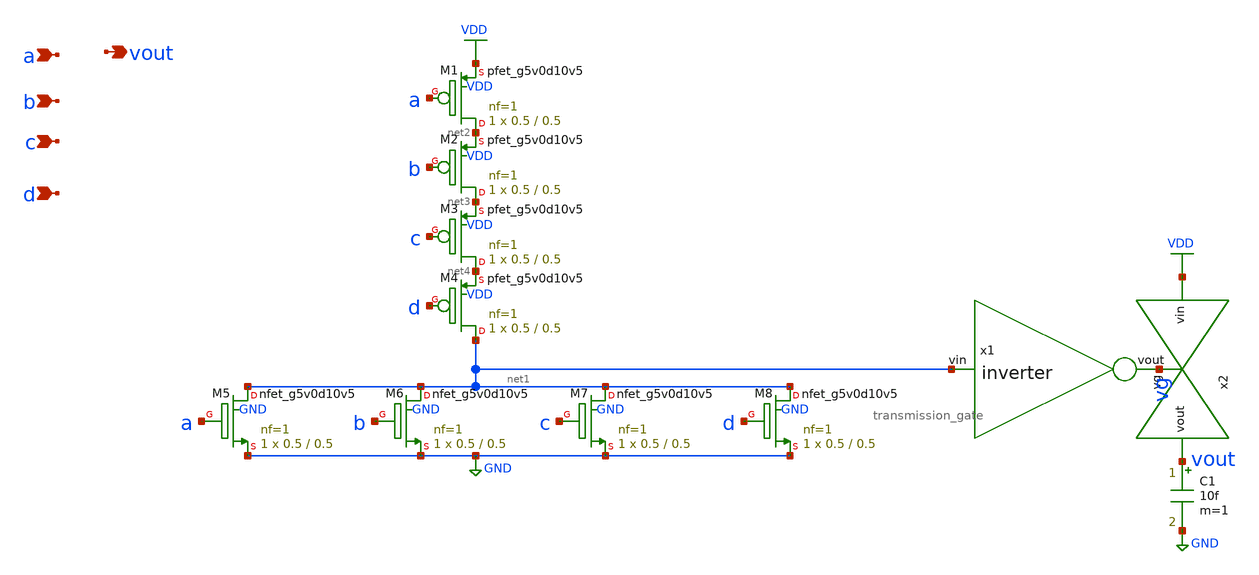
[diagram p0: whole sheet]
** sch_path: schematics/or4.sch
**.subckt or4 a b c d vout
*.ipin a
*.ipin b
*.ipin c
*.ipin d
*.opin vout
x1 vg net1 inverter
XM1 net2 a VDD VDD sky130_fd_pr__pfet_g5v0d10v5 L=0.5 W=0.5 nf=1 ad='int((nf+1)/2) * W/nf * 0.29' as='int((nf+2)/2) * W/nf * 0.29'
+ pd='2*int((nf+1)/2) * (W/nf + 0.29)' ps='2*int((nf+2)/2) * (W/nf + 0.29)' nrd='0.29 / W' nrs='0.29 / W'
+ sa=0 sb=0 sd=0 mult=1 m=1
XM5 net1 a GND GND sky130_fd_pr__nfet_g5v0d10v5 L=0.5 W=0.5 nf=1 ad='int((nf+1)/2) * W/nf * 0.29' as='int((nf+2)/2) * W/nf * 0.29'
+ pd='2*int((nf+1)/2) * (W/nf + 0.29)' ps='2*int((nf+2)/2) * (W/nf + 0.29)' nrd='0.29 / W' nrs='0.29 / W'
+ sa=0 sb=0 sd=0 mult=1 m=1
XM2 net3 b net2 VDD sky130_fd_pr__pfet_g5v0d10v5 L=0.5 W=0.5 nf=1 ad='int((nf+1)/2) * W/nf * 0.29' as='int((nf+2)/2) * W/nf * 0.29'
+ pd='2*int((nf+1)/2) * (W/nf + 0.29)' ps='2*int((nf+2)/2) * (W/nf + 0.29)' nrd='0.29 / W' nrs='0.29 / W'
+ sa=0 sb=0 sd=0 mult=1 m=1
XM3 net4 c net3 VDD sky130_fd_pr__pfet_g5v0d10v5 L=0.5 W=0.5 nf=1 ad='int((nf+1)/2) * W/nf * 0.29' as='int((nf+2)/2) * W/nf * 0.29'
+ pd='2*int((nf+1)/2) * (W/nf + 0.29)' ps='2*int((nf+2)/2) * (W/nf + 0.29)' nrd='0.29 / W' nrs='0.29 / W'
+ sa=0 sb=0 sd=0 mult=1 m=1
XM4 net1 d net4 VDD sky130_fd_pr__pfet_g5v0d10v5 L=0.5 W=0.5 nf=1 ad='int((nf+1)/2) * W/nf * 0.29' as='int((nf+2)/2) * W/nf * 0.29'
+ pd='2*int((nf+1)/2) * (W/nf + 0.29)' ps='2*int((nf+2)/2) * (W/nf + 0.29)' nrd='0.29 / W' nrs='0.29 / W'
+ sa=0 sb=0 sd=0 mult=1 m=1
XM6 net1 b GND GND sky130_fd_pr__nfet_g5v0d10v5 L=0.5 W=0.5 nf=1 ad='int((nf+1)/2) * W/nf * 0.29' as='int((nf+2)/2) * W/nf * 0.29'
+ pd='2*int((nf+1)/2) * (W/nf + 0.29)' ps='2*int((nf+2)/2) * (W/nf + 0.29)' nrd='0.29 / W' nrs='0.29 / W'
+ sa=0 sb=0 sd=0 mult=1 m=1
XM7 net1 c GND GND sky130_fd_pr__nfet_g5v0d10v5 L=0.5 W=0.5 nf=1 ad='int((nf+1)/2) * W/nf * 0.29' as='int((nf+2)/2) * W/nf * 0.29'
+ pd='2*int((nf+1)/2) * (W/nf + 0.29)' ps='2*int((nf+2)/2) * (W/nf + 0.29)' nrd='0.29 / W' nrs='0.29 / W'
+ sa=0 sb=0 sd=0 mult=1 m=1
XM8 net1 d GND GND sky130_fd_pr__nfet_g5v0d10v5 L=0.5 W=0.5 nf=1 ad='int((nf+1)/2) * W/nf * 0.29' as='int((nf+2)/2) * W/nf * 0.29'
+ pd='2*int((nf+1)/2) * (W/nf + 0.29)' ps='2*int((nf+2)/2) * (W/nf + 0.29)' nrd='0.29 / W' nrs='0.29 / W'
+ sa=0 sb=0 sd=0 mult=1 m=1
x2 VDD vout vg transmission_gate
C1 vout GND 10f m=1
**.ends

* expanding   symbol:  /media/sf_share/final_project/inverter.sym # of pins=2
** sym_path: schematics/inverter.sym
** sch_path: schematics/inverter.sch
.subckt inverter vout vin
*.ipin vin
*.opin vout
XM3 vout vin VDD VDD sky130_fd_pr__pfet_g5v0d10v5 L=0.5 W=0.5 nf=1 ad='int((nf+1)/2) * W/nf * 0.29' as='int((nf+2)/2) * W/nf * 0.29'
+ pd='2*int((nf+1)/2) * (W/nf + 0.29)' ps='2*int((nf+2)/2) * (W/nf + 0.29)' nrd='0.29 / W' nrs='0.29 / W'
+ sa=0 sb=0 sd=0 mult=1 m=1
XM5 vout vin GND GND sky130_fd_pr__nfet_g5v0d10v5 L=0.5 W=0.5 nf=1 ad='int((nf+1)/2) * W/nf * 0.29' as='int((nf+2)/2) * W/nf * 0.29'
+ pd='2*int((nf+1)/2) * (W/nf + 0.29)' ps='2*int((nf+2)/2) * (W/nf + 0.29)' nrd='0.29 / W' nrs='0.29 / W'
+ sa=0 sb=0 sd=0 mult=1 m=1
.ends


* expanding   symbol:  /media/sf_share/final_project/transmission_gate.sym # of pins=3
** sym_path: schematics/transmission_gate.sym
** sch_path: schematics/transmission_gate.sch
.subckt transmission_gate vin vout vg
*.ipin vin
*.ipin vg
*.opin vout
x1 vg_bar vg inverter
XM5 vin vg vout GND sky130_fd_pr__nfet_g5v0d10v5 L=0.5 W=0.5 nf=1 ad='int((nf+1)/2) * W/nf * 0.29' as='int((nf+2)/2) * W/nf * 0.29'
+ pd='2*int((nf+1)/2) * (W/nf + 0.29)' ps='2*int((nf+2)/2) * (W/nf + 0.29)' nrd='0.29 / W' nrs='0.29 / W'
+ sa=0 sb=0 sd=0 mult=1 m=1
XM7 vout vg_bar vin VDD sky130_fd_pr__pfet_g5v0d10v5 L=0.5 W=0.5 nf=1 ad='int((nf+1)/2) * W/nf * 0.29'
+ as='int((nf+2)/2) * W/nf * 0.29' pd='2*int((nf+1)/2) * (W/nf + 0.29)' ps='2*int((nf+2)/2) * (W/nf + 0.29)'
+ nrd='0.29 / W' nrs='0.29 / W' sa=0 sb=0 sd=0 mult=1 m=1
XM6 vout vg_bar GND GND sky130_fd_pr__nfet_g5v0d10v5 L=0.5 W=0.5 nf=1 ad='int((nf+1)/2) * W/nf * 0.29'
+ as='int((nf+2)/2) * W/nf * 0.29' pd='2*int((nf+1)/2) * (W/nf + 0.29)' ps='2*int((nf+2)/2) * (W/nf + 0.29)'
+ nrd='0.29 / W' nrs='0.29 / W' sa=0 sb=0 sd=0 mult=1 m=1
.ends

.GLOBAL VDD
.GLOBAL GND
.end
